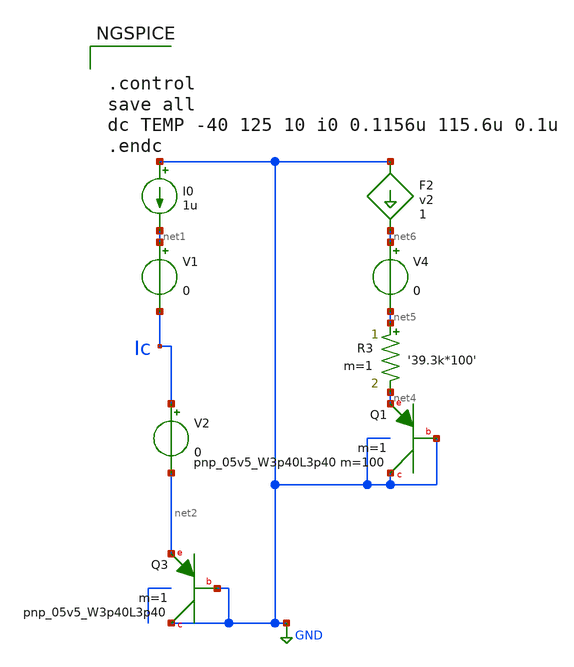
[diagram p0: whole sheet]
** sch_path: schematics/ptat_ctat_explore.sch
**.subckt ptat_ctat_explore
I0 GND net1 1u
XQ3 GND GND net2 sky130_fd_pr__pnp_05v5_W3p40L3p40 m=1
XQ1 GND GND net4 sky130_fd_pr__pnp_05v5_W3p40L3p40 m=100 m=1
R3 net5 net4 '39.3k*100' m=1
V1 net1 Ic 0
V2 Ic net2 0
F2 GND net6 v2 1
V4 net6 net5 0
**** begin user architecture code


.control
save all
dc TEMP -40 125 10 i0 0.1156u 115.6u 0.1u
.endc



.include $::SKYWATER_MODELS/cells/nfet_01v8/sky130_fd_pr__nfet_01v8__tt.corner.spice
.include $::SKYWATER_MODELS/cells/nfet_01v8_lvt/sky130_fd_pr__nfet_01v8_lvt__tt.corner.spice
.include $::SKYWATER_MODELS/cells/pfet_01v8/sky130_fd_pr__pfet_01v8__tt.corner.spice
.include $::SKYWATER_MODELS/cells/nfet_03v3_nvt/sky130_fd_pr__nfet_03v3_nvt__tt.corner.spice
.include $::SKYWATER_MODELS/cells/nfet_05v0_nvt/sky130_fd_pr__nfet_05v0_nvt__tt.corner.spice
.include $::SKYWATER_MODELS/cells/esd_nfet_01v8/sky130_fd_pr__esd_nfet_01v8__tt.corner.spice
.include $::SKYWATER_MODELS/cells/pfet_01v8_lvt/sky130_fd_pr__pfet_01v8_lvt__tt.corner.spice
.include $::SKYWATER_MODELS/cells/pfet_01v8_hvt/sky130_fd_pr__pfet_01v8_hvt__tt.corner.spice
.include $::SKYWATER_MODELS/cells/esd_pfet_g5v0d10v5/sky130_fd_pr__esd_pfet_g5v0d10v5__tt.corner.spice
.include $::SKYWATER_MODELS/cells/pfet_g5v0d10v5/sky130_fd_pr__pfet_g5v0d10v5__tt.corner.spice
.include $::SKYWATER_MODELS/cells/pfet_g5v0d16v0/sky130_fd_pr__pfet_g5v0d16v0__tt.corner.spice
.include $::SKYWATER_MODELS/cells/nfet_g5v0d10v5/sky130_fd_pr__nfet_g5v0d10v5__tt.corner.spice
.include $::SKYWATER_MODELS/cells/nfet_g5v0d16v0/sky130_fd_pr__nfet_g5v0d16v0__tt_discrete.corner.spice
.include $::SKYWATER_MODELS/cells/esd_nfet_g5v0d10v5/sky130_fd_pr__esd_nfet_g5v0d10v5__tt.corner.spice
.include $::SKYWATER_MODELS/models/corners/tt/nonfet.spice
* Mismatch parameters
.include $::SKYWATER_MODELS/cells/nfet_01v8/sky130_fd_pr__nfet_01v8__mismatch.corner.spice
.include $::SKYWATER_MODELS/cells/pfet_01v8/sky130_fd_pr__pfet_01v8__mismatch.corner.spice
.include $::SKYWATER_MODELS/cells/nfet_01v8_lvt/sky130_fd_pr__nfet_01v8_lvt__mismatch.corner.spice
.include $::SKYWATER_MODELS/cells/pfet_01v8_lvt/sky130_fd_pr__pfet_01v8_lvt__mismatch.corner.spice
.include $::SKYWATER_MODELS/cells/pfet_01v8_hvt/sky130_fd_pr__pfet_01v8_hvt__mismatch.corner.spice
.include $::SKYWATER_MODELS/cells/nfet_g5v0d10v5/sky130_fd_pr__nfet_g5v0d10v5__mismatch.corner.spice
.include $::SKYWATER_MODELS/cells/pfet_g5v0d10v5/sky130_fd_pr__pfet_g5v0d10v5__mismatch.corner.spice
.include $::SKYWATER_MODELS/cells/nfet_05v0_nvt/sky130_fd_pr__nfet_05v0_nvt__mismatch.corner.spice
.include $::SKYWATER_MODELS/cells/nfet_03v3_nvt/sky130_fd_pr__nfet_03v3_nvt__mismatch.corner.spice
* Resistor$::SKYWATER_MODELS/Capacitor
.include $::SKYWATER_MODELS/models/r+c/res_typical__cap_typical.spice
.include $::SKYWATER_MODELS/models/r+c/res_typical__cap_typical__lin.spice
* Special cells
.include $::SKYWATER_MODELS/models/corners/tt/specialized_cells.spice
* All models
.include $::SKYWATER_MODELS/models/all.spice
.include $::SKYWATER_MODELS/cells/pnp_05v5/sky130_fd_pr__pnp_05v5_W3p40L3p40.model.spice
* Corner
.include $::SKYWATER_MODELS/models/corners/tt/rf.spice

**** end user architecture code
**.ends
.GLOBAL GND
.end
